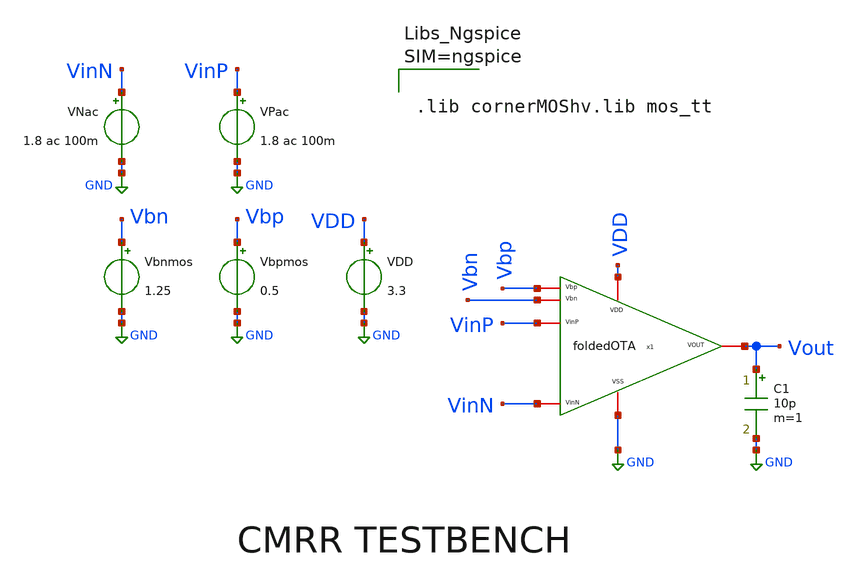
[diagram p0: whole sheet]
** sch_path: cmrr/CMRR-foldedOTA.sch
* v1_ideal_current_sources/schematic/foldedOTA.sch:
* (c) 2026 Fares Satouh
**.subckt CMRR-foldedOTA
VPac VinP GND 1.8 ac 100m
VNac VinN GND 1.8 ac 100m
Vbnmos Vbn GND 1.25
Vbpmos Vbp GND 0.5
VDD VDD GND 3.3
x1 VDD Vbp Vout VinP VinN Vbn GND foldedOTA
C1 Vout GND 10p m=1
**** begin user architecture code



.lib cornerMOShv.lib mos_tt





.control
close all
destroy all

ac dec 20 1 500Meg
let gain_cm_db = db(Vout/VinP)
meas ac acm_dc_gain find gain_cm_db at=1

alter VNac ac = -100m
ac dec 20 1 200G
let VinDiff = v(VinP) - v(VinN)
let gain_dm_db = db(Vout/VinDiff)
meas ac adm_dc_gain find gain_dm_db at=1

let cmrr_dc   = adm_dc_gain - ac1.acm_dc_gain
let cmrr_full = gain_dm_db  - ac1.gain_cm_db

echo
echo '================ CMRR RESULTS ================'
print adm_dc_gain
print ac1.acm_dc_gain
print cmrr_dc
echo '================================================'

* --- plots ---
plot ac1.gain_cm_db gain_dm_db ylabel 'Gain (dB)' xlog title 'Common-Mode vs Differential Gain'
plot cmrr_full ylabel 'CMRR (dB)' xlog title 'CMRR vs Frequency'

.endc


**** end user architecture code
**.ends

* expanding   symbol:  foldedOTA.sym # of pins=7
** sym_path: v1_ideal_current_sources/schematic/foldedOTA.sym
** sch_path: v1_ideal_current_sources/schematic/foldedOTA.sch
.subckt foldedOTA VDD Vbp VOUT VinP VinN Vbn VSS
*.iopin VDD
*.iopin VSS
*.iopin VOUT
*.iopin Vbp
*.iopin Vbn
*.iopin VinN
*.iopin VinP
XM1 net2 VinP net1 VSS sg13_hv_nmos w=28u l=1u ng=4 m=1 mm_ok=1
XM2 net3 VinN net1 VSS sg13_hv_nmos w=28u l=1u ng=4 m=1 mm_ok=1
XM3 net1 net8 VSS VSS sg13_hv_nmos w=15u l=1u ng=3 m=1 mm_ok=1
XM4 net2 net7 VDD VDD sg13_hv_pmos w=14u l=1u ng=2 m=1 mm_ok=1
XM5 net3 net7 VDD VDD sg13_hv_pmos w=14u l=1u ng=2 m=1 mm_ok=1
XM6 net4 Vbp net2 VDD sg13_hv_pmos w=2u l=1u ng=1 m=1 mm_ok=1
XM7 VOUT Vbp net3 VDD sg13_hv_pmos w=2u l=1u ng=1 m=1 mm_ok=1
XM8 net4 Vbn net5 VSS sg13_hv_nmos w=7u l=1u ng=1 m=1 mm_ok=1
XM9 VOUT Vbn net6 VSS sg13_hv_nmos w=7u l=1u ng=1 m=1 mm_ok=1
XM10 net5 net4 VSS VSS sg13_hv_nmos w=7u l=1u ng=1 m=1 mm_ok=1
XM11 net6 net4 VSS VSS sg13_hv_nmos w=7u l=1u ng=1 m=1 mm_ok=1
XM12 net8 net8 VSS VSS sg13_hv_nmos w=15u l=1u ng=3 m=1 mm_ok=1
I0 VDD net8 50u
XM13 net7 net7 VDD VDD sg13_hv_pmos w=14u l=1u ng=2 m=1 mm_ok=1
I1 net7 VSS 50u
.ends

.GLOBAL GND
.end
